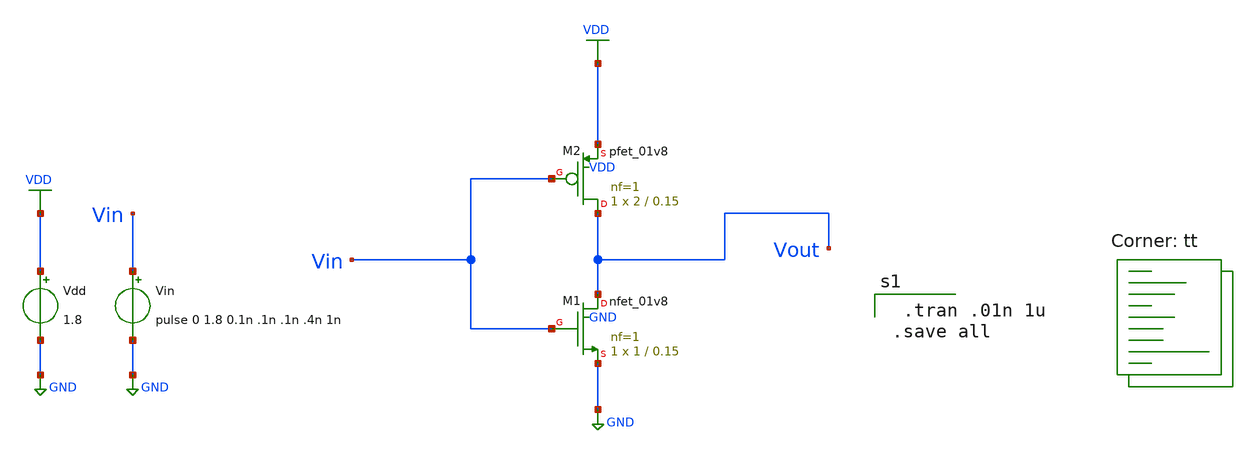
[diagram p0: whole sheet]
** sch_path: delay_cell/inv.sch
**.subckt inv
XM1 Vout Vin GND GND sky130_fd_pr__nfet_01v8 L=0.15 W=1 nf=1 ad='int((nf+1)/2) * W/nf * 0.29' as='int((nf+2)/2) * W/nf * 0.29'
+ pd='2*int((nf+1)/2) * (W/nf + 0.29)' ps='2*int((nf+2)/2) * (W/nf + 0.29)' nrd='0.29 / W' nrs='0.29 / W'
+ sa=0 sb=0 sd=0 mult=1 m=1
XM2 Vout Vin VDD VDD sky130_fd_pr__pfet_01v8 L=0.15 W=2 nf=1 ad='int((nf+1)/2) * W/nf * 0.29' as='int((nf+2)/2) * W/nf * 0.29'
+ pd='2*int((nf+1)/2) * (W/nf + 0.29)' ps='2*int((nf+2)/2) * (W/nf + 0.29)' nrd='0.29 / W' nrs='0.29 / W'
+ sa=0 sb=0 sd=0 mult=1 m=1
Vin Vin GND pulse 0 1.8 0.1n .1n .1n .4n 1n
Vdd VDD GND 1.8
**** begin user architecture code
.lib $::SKYWATER_MODELS/sky130.lib.spice tt

 .tran .01n 1u
.save all

**** end user architecture code
**.ends
.GLOBAL GND
.GLOBAL VDD
.end
